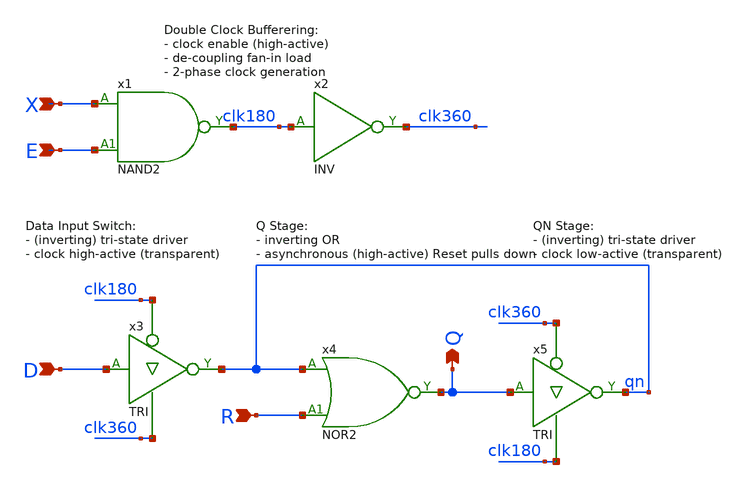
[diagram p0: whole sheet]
** sch_path: Sources/crafted/LATPER.sch
**.subckt LATPER X D Q E R
*.ipin X
*.ipin D
*.opin Q
*.ipin E
*.ipin R
x1 X E clk180 VDD GND NAND2 Wmin=1.5u Lmin=1u g=2 m=1
x2 clk180 clk360 VDD GND INV Wmin=1.5u Lmin=1u g=2 m=1
x3 D clk180 clk360 qn VDD GND TRI Wmin=1.5u Lmin=1u g=2 m=1
x5 Q clk360 clk180 qn VDD GND TRI Wmin=1.5u Lmin=1u g=2 m=1
x4 qn R Q VDD GND NOR2 Wmin=1.5u Lmin=1u g=2 m=1
**.ends
.end
